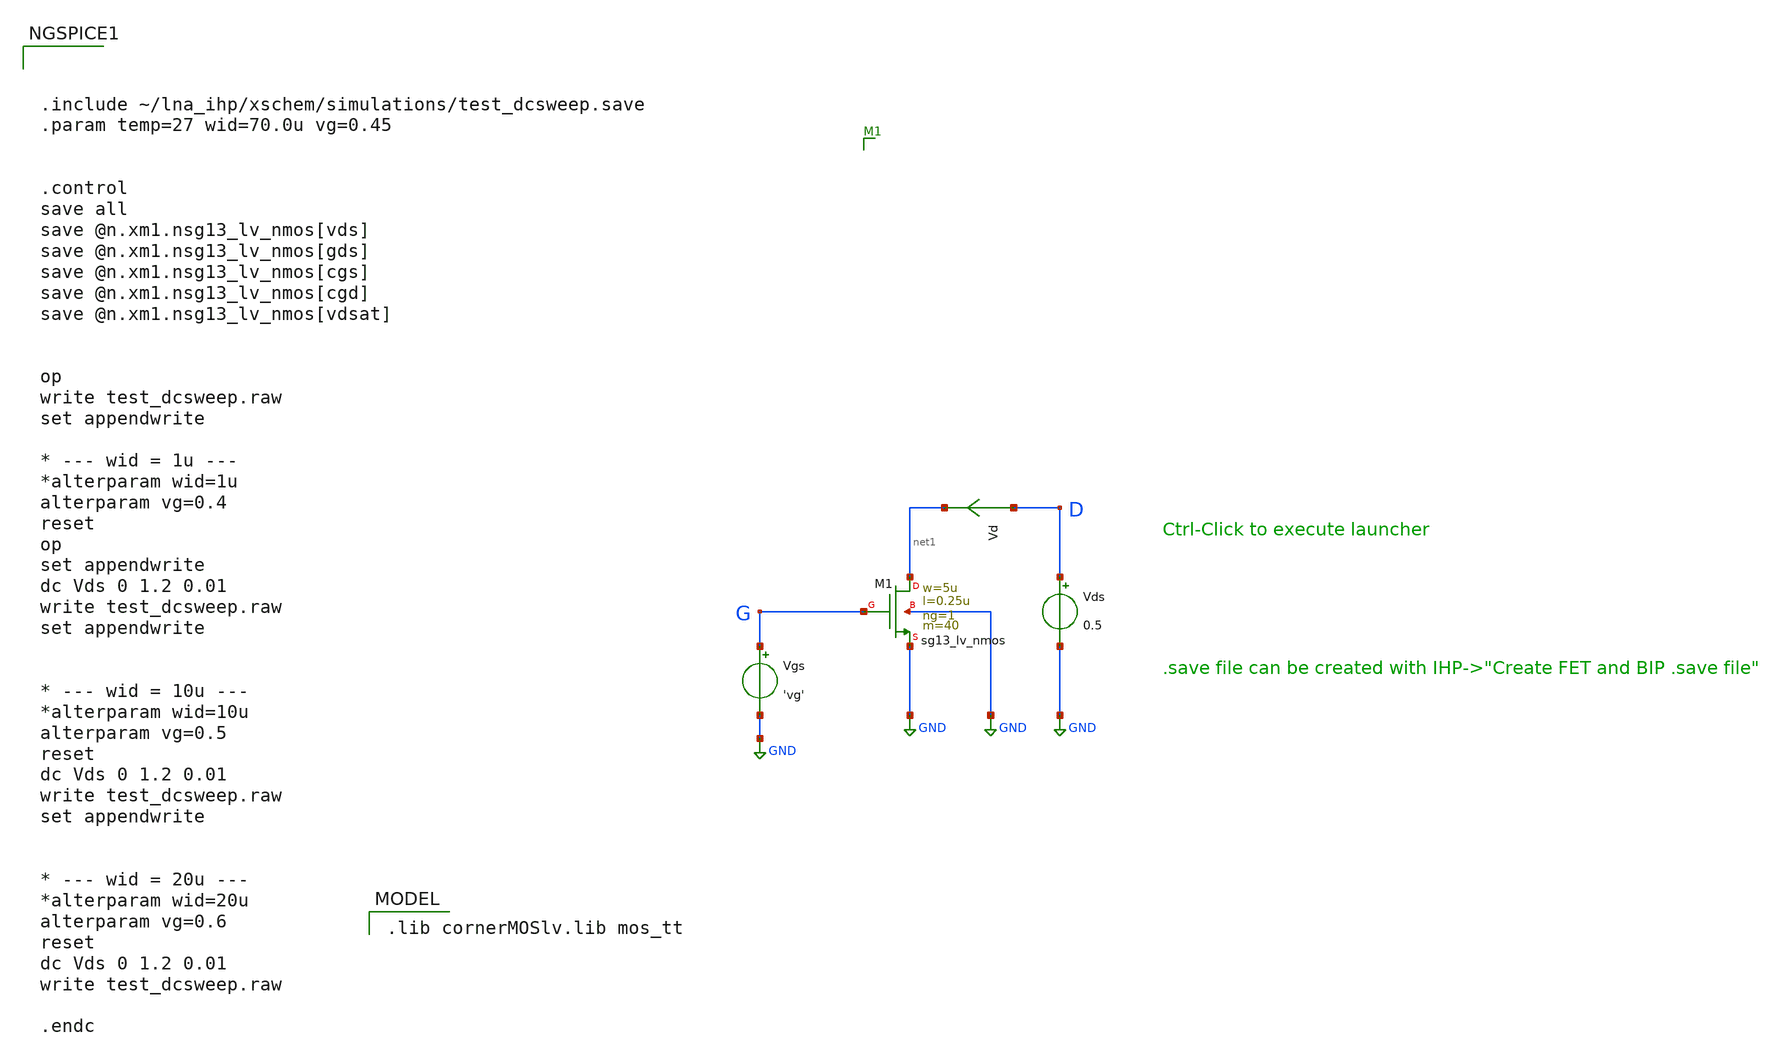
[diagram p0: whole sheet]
** sch_path: xschem/test_dcsweep.sch
**.subckt test_dcsweep
Vgs G GND 'vg'
Vds D GND 0.5
Vd D net1 0
.save i(vd)
XM1 net1 G GND GND sg13_lv_nmos w=5u l=0.25u ng=1 m=40 mm_ok=1
**** begin user architecture code
 .lib cornerMOSlv.lib mos_tt




.include ~/lna_ihp/xschem/simulations/test_dcsweep.save
.param temp=27 wid=70.0u vg=0.45


.control
save all
save @n.xm1.nsg13_lv_nmos[vds]
save @n.xm1.nsg13_lv_nmos[gds]
save @n.xm1.nsg13_lv_nmos[cgs]
save @n.xm1.nsg13_lv_nmos[cgd]
save @n.xm1.nsg13_lv_nmos[vdsat]


op
write test_dcsweep.raw
set appendwrite

* --- wid = 1u ---
*alterparam wid=1u
alterparam vg=0.4
reset
op
set appendwrite
dc Vds 0 1.2 0.01
write test_dcsweep.raw
set appendwrite


* --- wid = 10u ---
*alterparam wid=10u
alterparam vg=0.5
reset
dc Vds 0 1.2 0.01
write test_dcsweep.raw
set appendwrite


* --- wid = 20u ---
*alterparam wid=20u
alterparam vg=0.6
reset
dc Vds 0 1.2 0.01
write test_dcsweep.raw

.endc



**** end user architecture code
**.ends
.GLOBAL GND
.end
